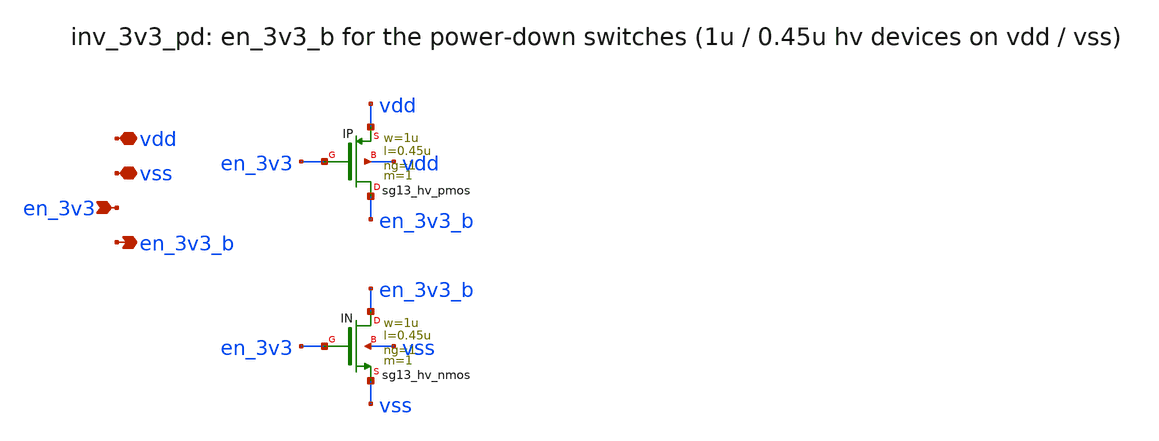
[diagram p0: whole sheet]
** sch_path: sudelbuecher/design_considerations/consolidation/reference_sheets_2026-10-20/macros/d2s_bias_sel_pd/schematic/xschem/inv_3v3_pd.sch
**.subckt inv_3v3_pd vdd vss en_3v3 en_3v3_b
*.iopin vdd
*.iopin vss
*.ipin en_3v3
*.opin en_3v3_b
XIP en_3v3_b en_3v3 vdd vdd sg13_hv_pmos w=1u l=0.45u ng=1 m=1 mm_ok=1
XIN en_3v3_b en_3v3 vss vss sg13_hv_nmos w=1u l=0.45u ng=1 m=1 mm_ok=1
**.ends
.end
